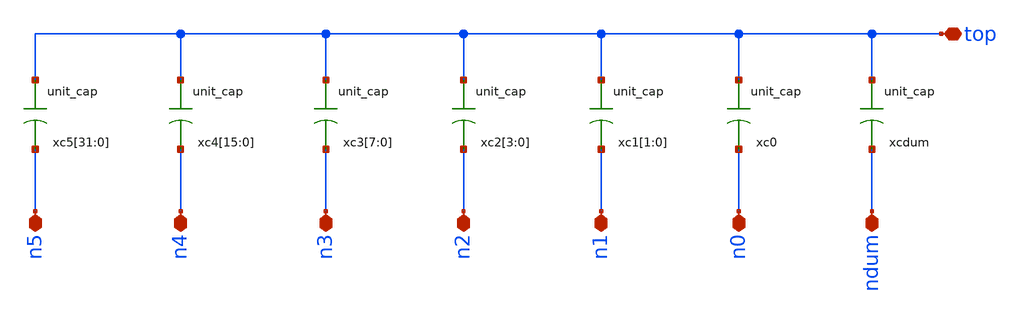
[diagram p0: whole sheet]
** sch_path: xschem/adc/carry.sch
**.subckt carry n5 n4 n3 n2 n1 n0 ndum top
*.iopin n5
*.iopin n4
*.iopin n3
*.iopin n2
*.iopin n1
*.iopin n0
*.iopin ndum
*.iopin top
xc0 top n0 unit_cap
xcdum top ndum unit_cap
xc1[1] top n1 unit_cap
xc1[0] top n1 unit_cap
xc2[3] top n2 unit_cap
xc2[2] top n2 unit_cap
xc2[1] top n2 unit_cap
xc2[0] top n2 unit_cap
xc3[7] top n3 unit_cap
xc3[6] top n3 unit_cap
xc3[5] top n3 unit_cap
xc3[4] top n3 unit_cap
xc3[3] top n3 unit_cap
xc3[2] top n3 unit_cap
xc3[1] top n3 unit_cap
xc3[0] top n3 unit_cap
xc4[15] top n4 unit_cap
xc4[14] top n4 unit_cap
xc4[13] top n4 unit_cap
xc4[12] top n4 unit_cap
xc4[11] top n4 unit_cap
xc4[10] top n4 unit_cap
xc4[9] top n4 unit_cap
xc4[8] top n4 unit_cap
xc4[7] top n4 unit_cap
xc4[6] top n4 unit_cap
xc4[5] top n4 unit_cap
xc4[4] top n4 unit_cap
xc4[3] top n4 unit_cap
xc4[2] top n4 unit_cap
xc4[1] top n4 unit_cap
xc4[0] top n4 unit_cap
xc5[31] top n5 unit_cap
xc5[30] top n5 unit_cap
xc5[29] top n5 unit_cap
xc5[28] top n5 unit_cap
xc5[27] top n5 unit_cap
xc5[26] top n5 unit_cap
xc5[25] top n5 unit_cap
xc5[24] top n5 unit_cap
xc5[23] top n5 unit_cap
xc5[22] top n5 unit_cap
xc5[21] top n5 unit_cap
xc5[20] top n5 unit_cap
xc5[19] top n5 unit_cap
xc5[18] top n5 unit_cap
xc5[17] top n5 unit_cap
xc5[16] top n5 unit_cap
xc5[15] top n5 unit_cap
xc5[14] top n5 unit_cap
xc5[13] top n5 unit_cap
xc5[12] top n5 unit_cap
xc5[11] top n5 unit_cap
xc5[10] top n5 unit_cap
xc5[9] top n5 unit_cap
xc5[8] top n5 unit_cap
xc5[7] top n5 unit_cap
xc5[6] top n5 unit_cap
xc5[5] top n5 unit_cap
xc5[4] top n5 unit_cap
xc5[3] top n5 unit_cap
xc5[2] top n5 unit_cap
xc5[1] top n5 unit_cap
xc5[0] top n5 unit_cap
**.ends

* expanding   symbol:  adc/unit_cap.sym # of pins=2
** sym_path: xschem/adc/unit_cap.sym
** sch_path: xschem/adc/unit_cap.sch
.subckt unit_cap cp cn
*.iopin cp
*.iopin cn
C1 cp cn 2.6f m=1
.ends

.end
